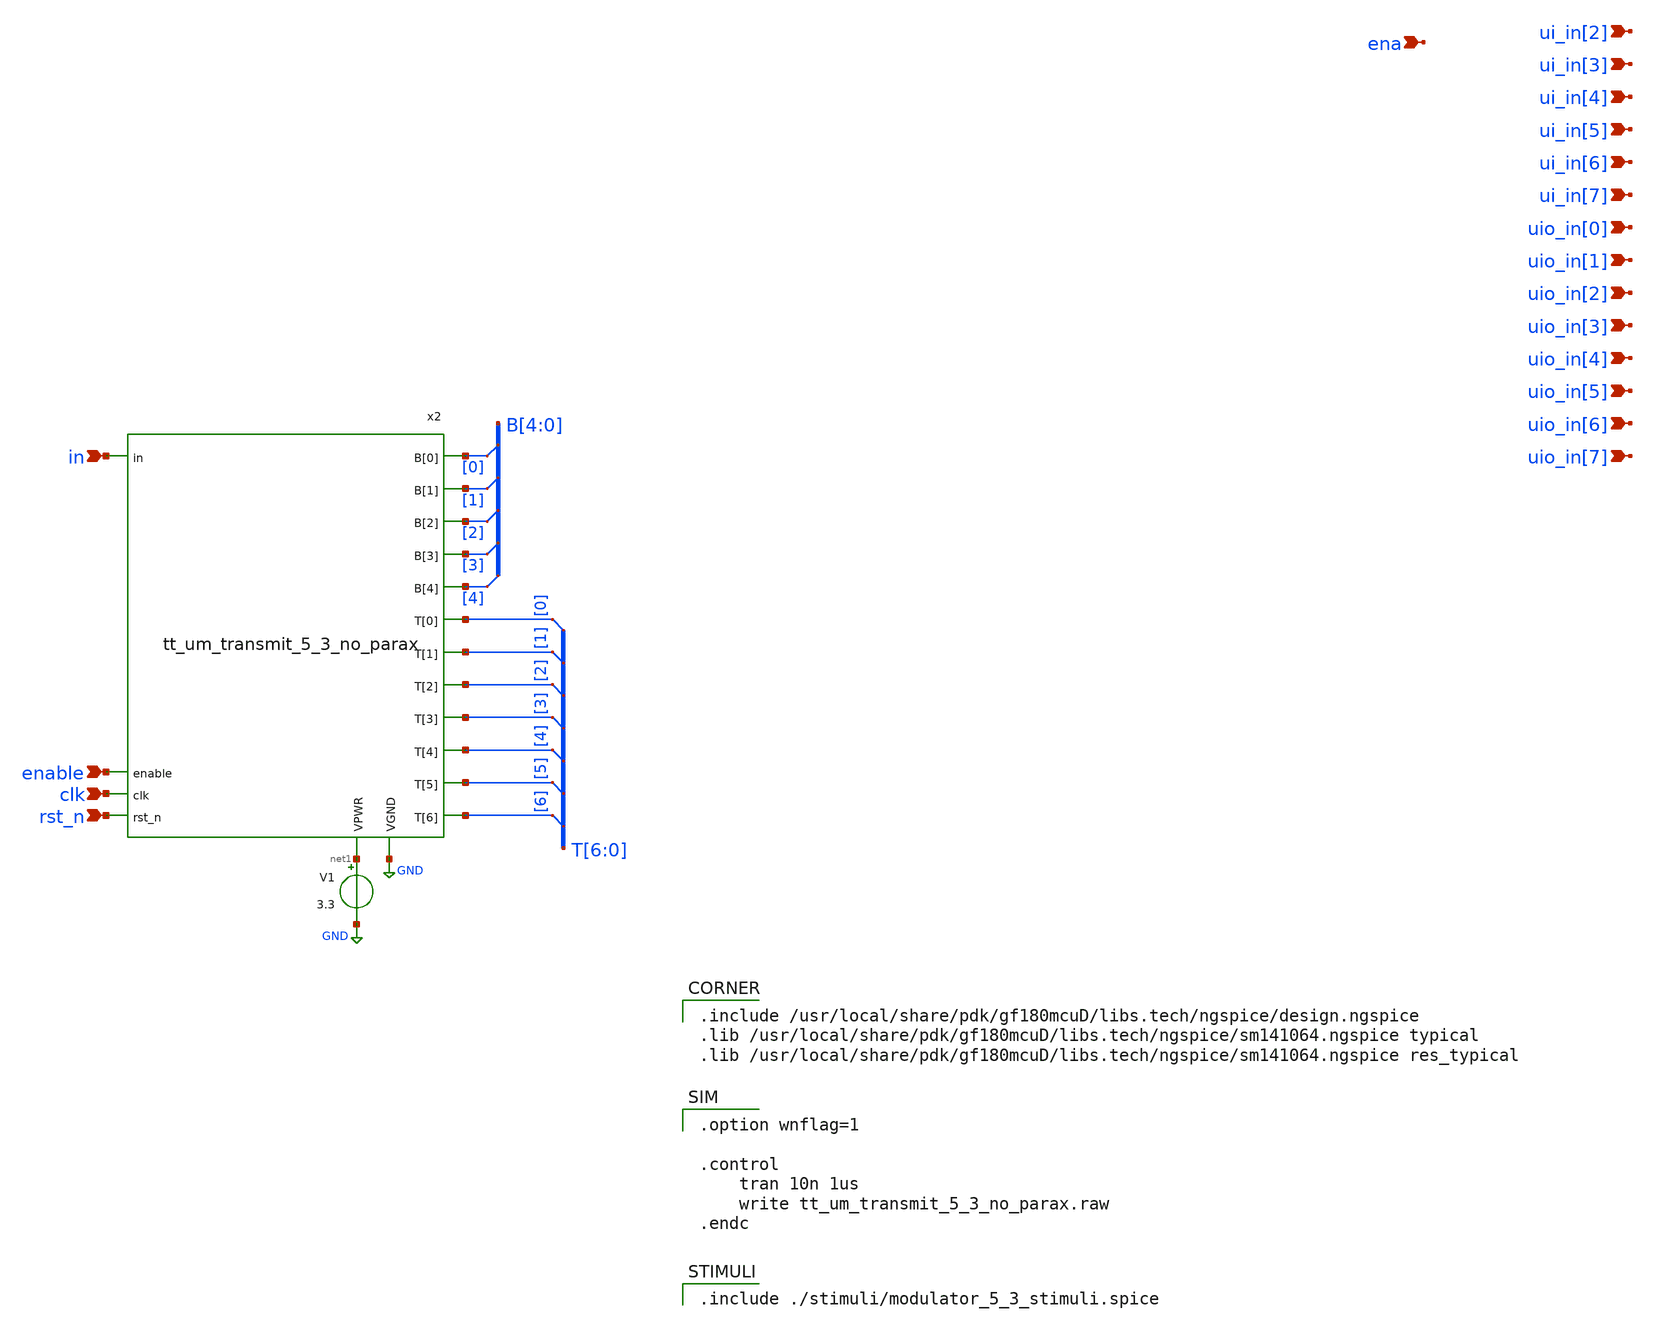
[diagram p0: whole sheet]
** sch_path: xschem/tb_transmit_no_parax.sch
**.subckt tb_transmit_no_parax in enable clk rst_n ui_in[2] ui_in[3] ui_in[4] ui_in[5] ui_in[6]
*+ ui_in[7] uio_in[0] uio_in[1] uio_in[2] uio_in[3] uio_in[4] uio_in[5] uio_in[6] uio_in[7] ena
*.ipin in
*.ipin enable
*.ipin clk
*.ipin rst_n
*.ipin ui_in[2]
*.ipin ui_in[3]
*.ipin ui_in[4]
*.ipin ui_in[5]
*.ipin ui_in[6]
*.ipin ui_in[7]
*.ipin uio_in[0]
*.ipin uio_in[1]
*.ipin uio_in[2]
*.ipin uio_in[3]
*.ipin uio_in[4]
*.ipin uio_in[5]
*.ipin uio_in[6]
*.ipin uio_in[7]
*.ipin ena
V1 net1 GND 3.3
* tap: B[4:0] --> B[0]
* tap: B[4:0] --> B[1]
* tap: B[4:0] --> B[2]
* tap: B[4:0] --> B[3]
* tap: B[4:0] --> B[4]
* tap: T[6:0] --> T[0]
* tap: T[6:0] --> T[1]
* tap: T[6:0] --> T[2]
* tap: T[6:0] --> T[3]
* tap: T[6:0] --> T[4]
* tap: T[6:0] --> T[5]
* tap: T[6:0] --> T[6]
x2 B[0] B[1] B[2] B[3] B[4] T[0] T[1] T[2] T[3] T[4] T[5] T[6] GND net1 clk enable in rst_n
+ tt_um_transmit_5_3_no_parax
**** begin user architecture code

.option wnflag=1

.control
    tran 10n 1us
    write tt_um_transmit_5_3_no_parax.raw
.endc



.include ./stimuli/modulator_5_3_stimuli.spice


.include /usr/local/share/pdk/gf180mcuD/libs.tech/ngspice/design.ngspice
.lib /usr/local/share/pdk/gf180mcuD/libs.tech/ngspice/sm141064.ngspice typical
.lib /usr/local/share/pdk/gf180mcuD/libs.tech/ngspice/sm141064.ngspice res_typical

**** end user architecture code
**.ends

* expanding   symbol:  tt_um_transmit_5_3_no_parax.sym # of pins=18
** sym_path: xschem/tt_um_transmit_5_3_no_parax.sym
.include ../../mag/spice/tt_um_transmit_5_3_no_parax.spice
.GLOBAL GND
.end
